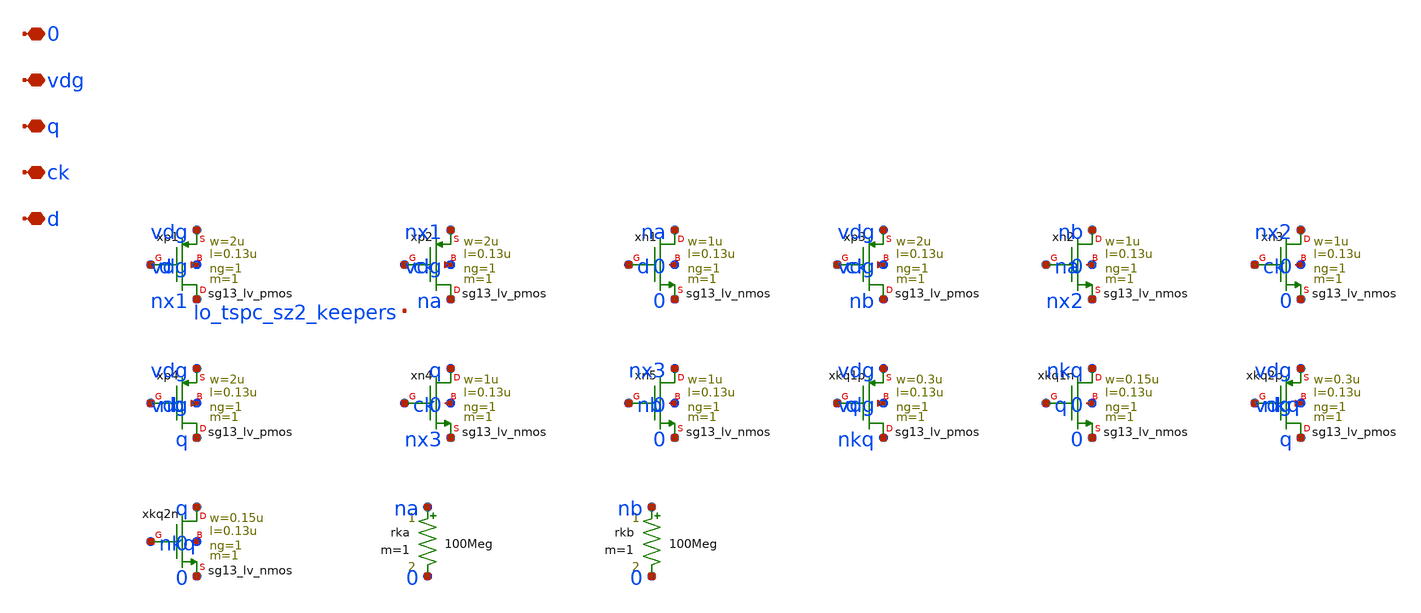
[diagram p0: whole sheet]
** sch_path: analog/lo/sch/lo_tspc.sch
**.subckt lo_tspc d ck q vdg 0
*.iopin d
*.iopin ck
*.iopin q
*.iopin vdg
*.iopin 0
Xxp1 nx1 d vdg vdg sg13_lv_pmos w=2u l=0.13u ng=1 m=1 mm_ok=1
Xxp2 na ck nx1 vdg sg13_lv_pmos w=2u l=0.13u ng=1 m=1 mm_ok=1
Xxn1 na d 0 0 sg13_lv_nmos w=1u l=0.13u ng=1 m=1 mm_ok=1
Xxp3 nb ck vdg vdg sg13_lv_pmos w=2u l=0.13u ng=1 m=1 mm_ok=1
Xxn2 nb na nx2 0 sg13_lv_nmos w=1u l=0.13u ng=1 m=1 mm_ok=1
Xxn3 nx2 ck 0 0 sg13_lv_nmos w=1u l=0.13u ng=1 m=1 mm_ok=1
Xxp4 q nb vdg vdg sg13_lv_pmos w=2u l=0.13u ng=1 m=1 mm_ok=1
Xxn4 q ck nx3 0 sg13_lv_nmos w=1u l=0.13u ng=1 m=1 mm_ok=1
Xxn5 nx3 nb 0 0 sg13_lv_nmos w=1u l=0.13u ng=1 m=1 mm_ok=1
Xxkq1p nkq q vdg vdg sg13_lv_pmos w=0.3u l=0.13u ng=1 m=1 mm_ok=1
Xxkq1n nkq q 0 0 sg13_lv_nmos w=0.15u l=0.13u ng=1 m=1 mm_ok=1
Xxkq2p q nkq vdg vdg sg13_lv_pmos w=0.3u l=0.13u ng=1 m=1 mm_ok=1
Xxkq2n q nkq 0 0 sg13_lv_nmos w=0.15u l=0.13u ng=1 m=1 mm_ok=1
rka na 0 100Meg m=1
rkb nb 0 100Meg m=1
**.ends
.end
